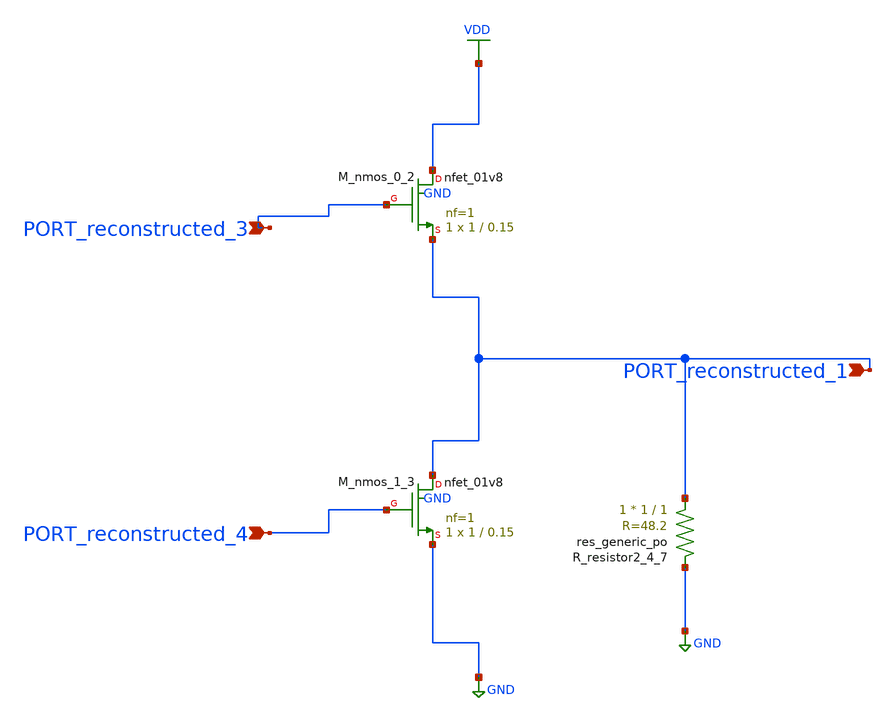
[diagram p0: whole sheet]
** sch_path: schematics/AMSNet/104.sch
**.subckt 104 PORT_reconstructed_4 PORT_reconstructed_3 PORT_reconstructed_1
*.ipin PORT_reconstructed_4
*.ipin PORT_reconstructed_3
*.ipin PORT_reconstructed_1
XM_nmos_0_2 VDD PORT_reconstructed_3 PORT_reconstructed_1 GND sky130_fd_pr__nfet_01v8 L=0.15 W=1 nf=1
+ ad='int((1 + 1)/2) * 1 / 1 * 0.29' as='int((1 + 2)/2) * 1 / 1 * 0.29' pd='2*int((1 + 1)/2) * (1 / 1 + 0.29)'
+ ps='2*int((1 + 2)/2) * (1 / 1 + 0.29)' nrd='0.29 / 1 ' nrs='0.29 / 1 ' sa=0 sb=0 sd=0 mult=1 m=1
XM_nmos_1_3 PORT_reconstructed_1 PORT_reconstructed_4 GND GND sky130_fd_pr__nfet_01v8 L=0.15 W=1 nf=1
+ ad='int((1 + 1)/2) * 1 / 1 * 0.29' as='int((1 + 2)/2) * 1 / 1 * 0.29' pd='2*int((1 + 1)/2) * (1 / 1 + 0.29)'
+ ps='2*int((1 + 2)/2) * (1 / 1 + 0.29)' nrd='0.29 / 1 ' nrs='0.29 / 1 ' sa=0 sb=0 sd=0 mult=1 m=1
XR_resistor2_4_7 PORT_reconstructed_1 GND sky130_fd_pr__res_generic_po W=1 L=1 m=1
**.ends
.GLOBAL GND
.GLOBAL VDD
.end
